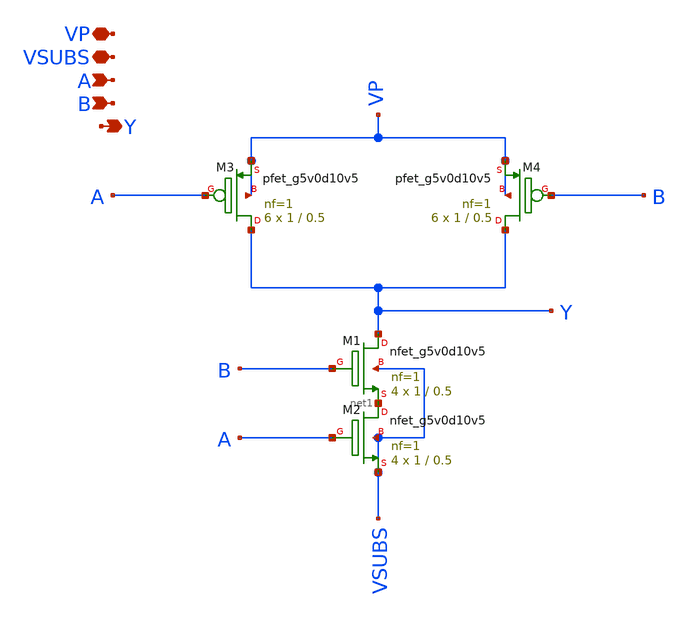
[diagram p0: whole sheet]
** sch_path: xschem/nand2_x6.sch
**.subckt nand2_x6 VP VSUBS A B Y
*.iopin VP
*.iopin VSUBS
*.ipin A
*.ipin B
*.opin Y
XM1 Y B net1 VSUBS sky130_fd_pr__nfet_g5v0d10v5 L=0.5 W=1 nf=1 ad='int((nf+1)/2) * W/nf * 0.29' as='int((nf+2)/2) * W/nf * 0.29'
+ pd='2*int((nf+1)/2) * (W/nf + 0.29)' ps='2*int((nf+2)/2) * (W/nf + 0.29)' nrd='0.29 / W' nrs='0.29 / W'
+ sa=0 sb=0 sd=0 mult=4 m=4
XM2 net1 A VSUBS VSUBS sky130_fd_pr__nfet_g5v0d10v5 L=0.5 W=1 nf=1 ad='int((nf+1)/2) * W/nf * 0.29' as='int((nf+2)/2) * W/nf * 0.29'
+ pd='2*int((nf+1)/2) * (W/nf + 0.29)' ps='2*int((nf+2)/2) * (W/nf + 0.29)' nrd='0.29 / W' nrs='0.29 / W'
+ sa=0 sb=0 sd=0 mult=4 m=4
XM3 Y A VP VP sky130_fd_pr__pfet_g5v0d10v5 L=0.5 W=1 nf=1 ad='int((nf+1)/2) * W/nf * 0.29' as='int((nf+2)/2) * W/nf * 0.29'
+ pd='2*int((nf+1)/2) * (W/nf + 0.29)' ps='2*int((nf+2)/2) * (W/nf + 0.29)' nrd='0.29 / W' nrs='0.29 / W'
+ sa=0 sb=0 sd=0 mult=6 m=6
XM4 Y B VP VP sky130_fd_pr__pfet_g5v0d10v5 L=0.5 W=1 nf=1 ad='int((nf+1)/2) * W/nf * 0.29' as='int((nf+2)/2) * W/nf * 0.29'
+ pd='2*int((nf+1)/2) * (W/nf + 0.29)' ps='2*int((nf+2)/2) * (W/nf + 0.29)' nrd='0.29 / W' nrs='0.29 / W'
+ sa=0 sb=0 sd=0 mult=6 m=6
**.ends
.end
